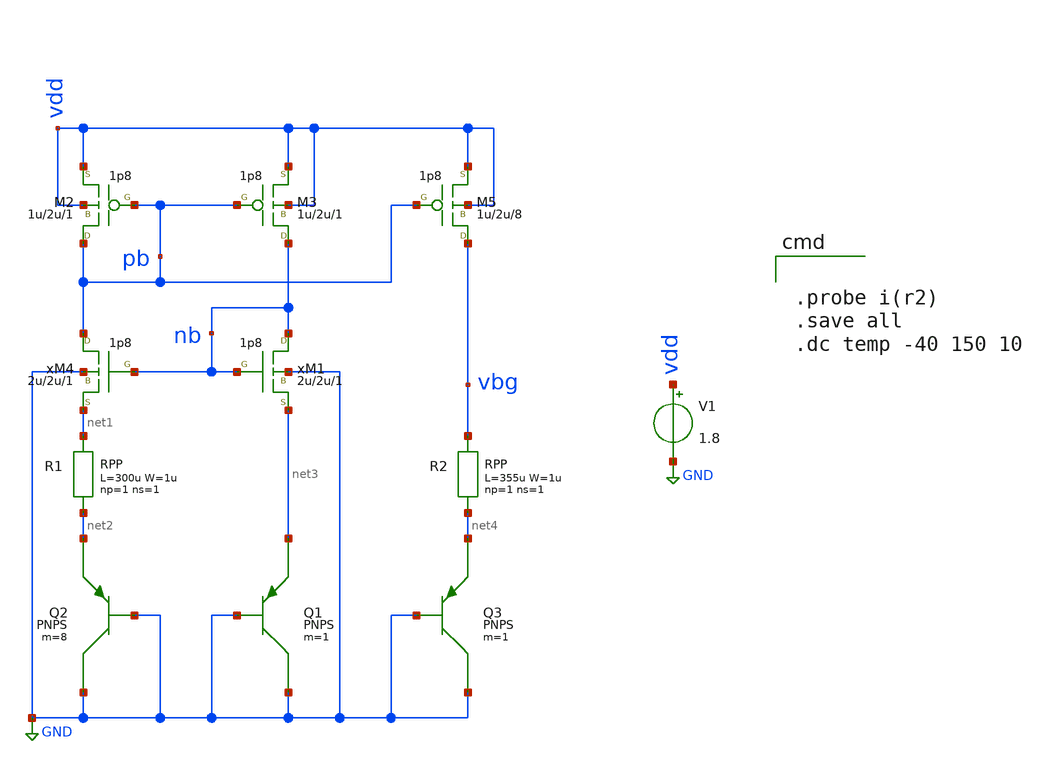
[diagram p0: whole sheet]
** sch_path: xschem/gen18_examples/bg.sch
**.subckt bg
xM1 nb nb net3 GND nmos18 w=2u l=2u m=1
M2 pb pb vdd vdd pmos18 w=1u l=2u m=1 ad='2*1u *0.18u' as='2*1u *0.18u' pd='2*(1u +2*0.18u)' ps='2*(1u +2*0.18u)'
V1 vdd GND 1.8
M3 nb pb vdd vdd pmos18 w=1u l=2u m=1 ad='2*1u *0.18u' as='2*1u *0.18u' pd='2*(1u +2*0.18u)' ps='2*(1u +2*0.18u)'
xM4 pb nb net1 GND nmos18 w=2u l=2u m=1
Q1 GND GND net3 PNPS m=1
Q2 GND GND net2 PNPS m=8
xR1 net1 net2 RPP W=1u L=300u np=1 ns=1
M5 vbg pb vdd vdd pmos18 w=1u l=2u m=8 ad='2*1u *0.18u' as='2*1u *0.18u' pd='2*(1u +2*0.18u)' ps='2*(1u +2*0.18u)'
Q3 GND GND net4 PNPS m=1
xR2 vbg net4 RPP W=1u L=355u np=1 ns=1
**** begin user architecture code

.probe i(r2)
.save all
.dc temp -40 150 10

.include  [path_head [abs_sym_path gen18/gen18models.sym] 3]/mdl/gen18.inc
**** end user architecture code
**.ends
.GLOBAL GND
.end
